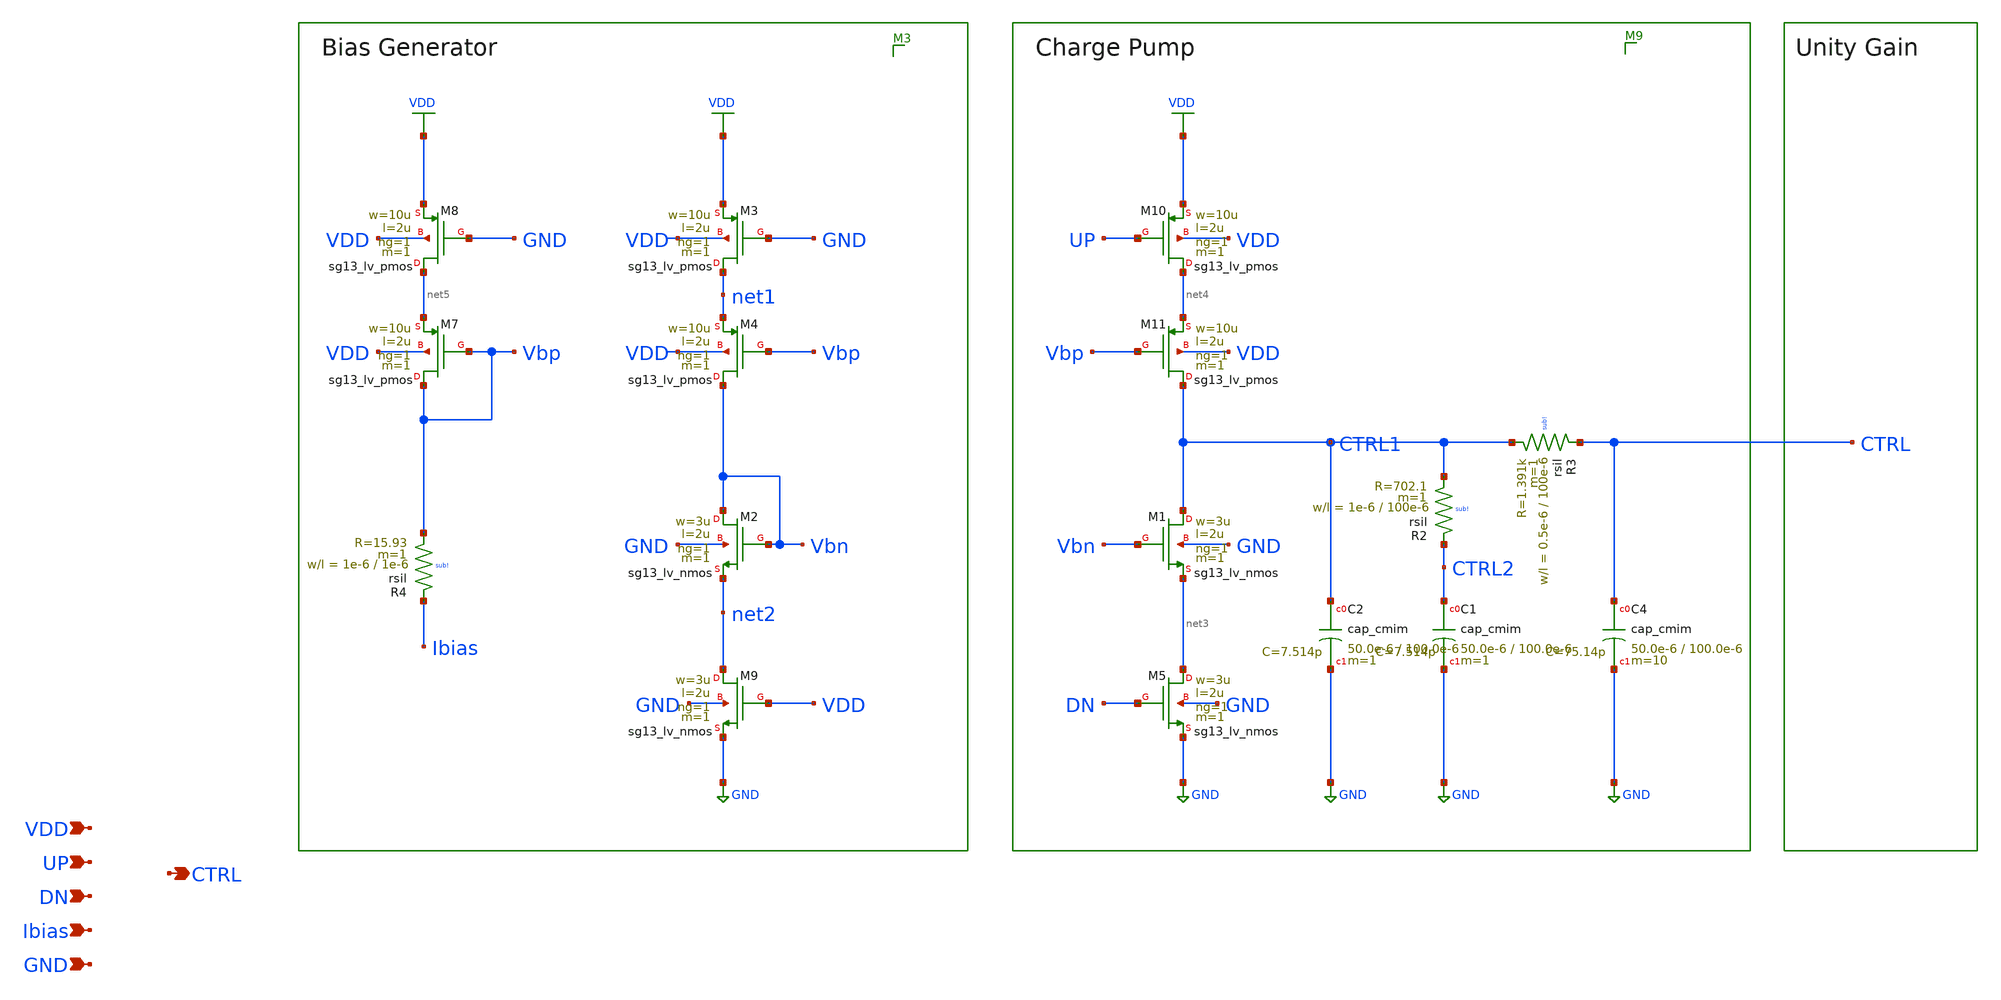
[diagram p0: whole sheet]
** sch_path: schematic/blocks/charge-pump/Top_CP.sch
**.subckt Top_CP CTRL UP VDD Ibias DN GND
*.opin CTRL
*.ipin UP
*.ipin VDD
*.ipin Ibias
*.ipin DN
*.ipin GND
XM2 Vbn Vbn net2 GND sg13_lv_nmos w=3u l=2u ng=1 m=1 mm_ok=1
XM8 net5 GND VDD VDD sg13_lv_pmos w=10u l=2u ng=1 m=1 mm_ok=1
XR3 CTRL CTRL1 sub! rsil w=0.5e-6 l=100e-6 m=1 mm_ok=1
XR2 CTRL2 CTRL1 sub! rsil w=1e-6 l=100e-6 m=1 mm_ok=1
XC4 CTRL GND cap_cmim w=50.0e-6 l=100.0e-6 m=10 mm_ok=1
XC1 CTRL2 GND cap_cmim w=50.0e-6 l=100.0e-6 m=1 mm_ok=1
XC2 CTRL1 GND cap_cmim w=50.0e-6 l=100.0e-6 m=1 mm_ok=1
XM7 Vbp Vbp net5 VDD sg13_lv_pmos w=10u l=2u ng=1 m=1 mm_ok=1
XM3 net1 GND VDD VDD sg13_lv_pmos w=10u l=2u ng=1 m=1 mm_ok=1
XM4 Vbn Vbp net1 VDD sg13_lv_pmos w=10u l=2u ng=1 m=1 mm_ok=1
XM10 net4 UP VDD VDD sg13_lv_pmos w=10u l=2u ng=1 m=1 mm_ok=1
XM11 CTRL1 Vbp net4 VDD sg13_lv_pmos w=10u l=2u ng=1 m=1 mm_ok=1
XM9 net2 VDD GND GND sg13_lv_nmos w=3u l=2u ng=1 m=1 mm_ok=1
XM1 CTRL1 Vbn net3 GND sg13_lv_nmos w=3u l=2u ng=1 m=1 mm_ok=1
XM5 net3 DN GND GND sg13_lv_nmos w=3u l=2u ng=1 m=1 mm_ok=1
XR4 Ibias Vbp sub! rsil w=1e-6 l=1e-6 m=1 mm_ok=1
**.ends
.GLOBAL GND
.GLOBAL VDD
.end
